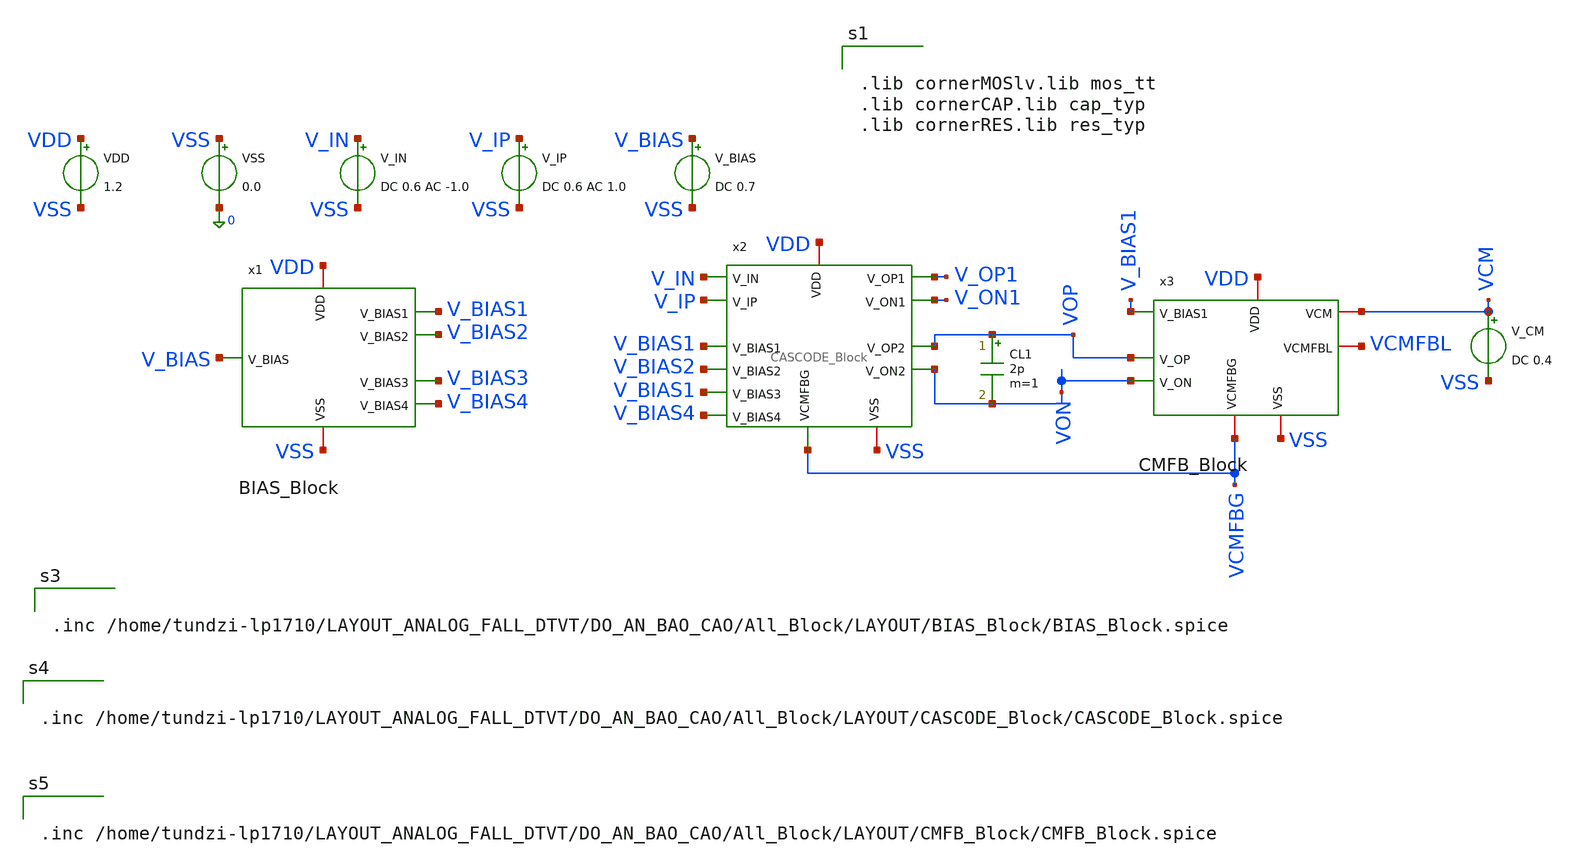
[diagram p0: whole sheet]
** sch_path: two-stage-ota-with-cmfb/Layout_PEX_PostSimulation/LAYOUT/SCHEMATIC_FOR_LAYOUT/Trans_PostSimulation.sch
**.subckt Trans_PostSimulation
VDD VDD VSS 1.2
VSS VSS 0 0.0
V_IN V_IN VSS DC 0.6 AC -1.0
V_IP V_IP VSS DC 0.6 AC 1.0
V_BIAS V_BIAS VSS DC 0.7
V_CM VCM VSS DC 0.4
CL1 VOP VON 2p m=1
x1 VDD VSS V_BIAS4 V_BIAS2 V_BIAS3 V_BIAS1 V_BIAS BIAS_Block
x2 VON VOP V_ON1 V_OP1 V_IN V_IP V_BIAS1 VSS V_BIAS4 V_BIAS1 VCMFBG VDD V_BIAS2 CASCODE_Block
x3 VDD V_BIAS1 VOP VON VCM VCMFBG VCMFBL VSS CMFB_Block
**** begin user architecture code


.lib cornerMOSlv.lib mos_tt
.lib cornerCAP.lib cap_typ
.lib cornerRES.lib res_typ




.inc /home/tundzi-lp1710/LAYOUT_ANALOG_FALL_DTVT/DO_AN_BAO_CAO/All_Block/LAYOUT/BIAS_Block/BIAS_Block.spice




.inc /home/tundzi-lp1710/LAYOUT_ANALOG_FALL_DTVT/DO_AN_BAO_CAO/All_Block/LAYOUT/CASCODE_Block/CASCODE_Block.spice




.inc /home/tundzi-lp1710/LAYOUT_ANALOG_FALL_DTVT/DO_AN_BAO_CAO/All_Block/LAYOUT/CMFB_Block/CMFB_Block.spice




* RUN STEP RESPONSE
.control
set color0=white
set color1=black

* Xung buoc nhay 0.5Vpp
alter @v_ip[pulse] = [ 0.475 0.725 10n 0.1n 0.1n 50n 100n ]
alter @v_in[pulse] = [ 0.725 0.475 10n 0.1n 0.1n 50n 100n ]

tran 20p 120n

let v_out_diff = v(vop) - v(von)
let v_in_diff  = v(v_ip) - v(v_in)
let sr_trace   = deriv(v_out_diff) / 1e6

* Do Slew Rate 20% - 80%
meas tran t_r20 when v_out_diff=-0.15 rise=1
meas tran t_r80 when v_out_diff=0.15 rise=1
let sr_rise = (0.3 / (t_r80 - t_r20)) / 1e6

meas tran t_f80 when v_out_diff=0.15 fall=1
meas tran t_f20 when v_out_diff=-0.15 fall=1
let sr_fall = (0.3 / (t_f20 - t_f80)) / 1e6

* Do Overshoot
meas tran v_max max v_out_diff from=10n to=60n
let overshoot_pct = ((v_max - 0.25) / 0.25) * 100

* Do Settling Time
meas tran t_settle_1pct when v_out_diff=0.2475 rise=1
meas tran t_settle_01pct when v_out_diff=0.24975 rise=1

print sr_rise sr_fall
print overshoot_pct
print t_settle_1pct t_settle_01pct

plot v_in_diff v_out_diff ylabel 'Voltage (V)' xlabel 'Time (s)' title 'Large-Signal Step Response'
plot sr_trace ylabel 'Slew Rate (V/us)' xlabel 'Time (s)' title 'Instantaneous Slew Rate'
.endc


**** end user architecture code
**.ends
.end
